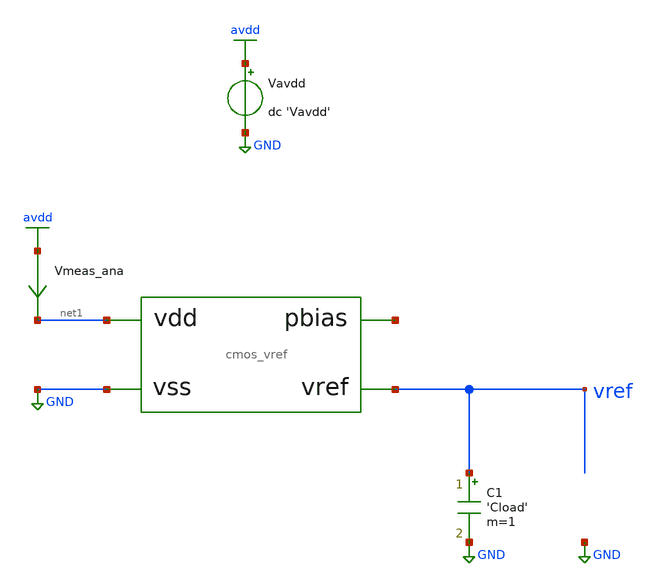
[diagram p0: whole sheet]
** sch_path: tb/cmos_vref/tb_vref_temp_sweep.sch
**.subckt tb_vref_temp_sweep
Vavdd avdd GND dc 'Vavdd'
C1 vref GND 'Cload' m=1
Vmeas_ana avdd net1 0
.save i(vmeas_ana)
X1 vref net1 GND net2 cmos_vref
**** begin user architecture code


.lib 'models_dir'/cornerMOShv.lib 'mos_corner'
.lib 'models_dir'/cornerMOSlv.lib 'mos_corner'
.lib 'models_dir'/cornerCAP.lib cap_typ
.option warn=1
.control
save vref
dc TEMP 'temp_min' 'temp_max' 5
set wr_singlescale
wrdata 'simpath'/'filename'_'N'.data V(vref)
quit
.endc


**** end user architecture code
**.ends
.GLOBAL avdd
.GLOBAL GND
.end
